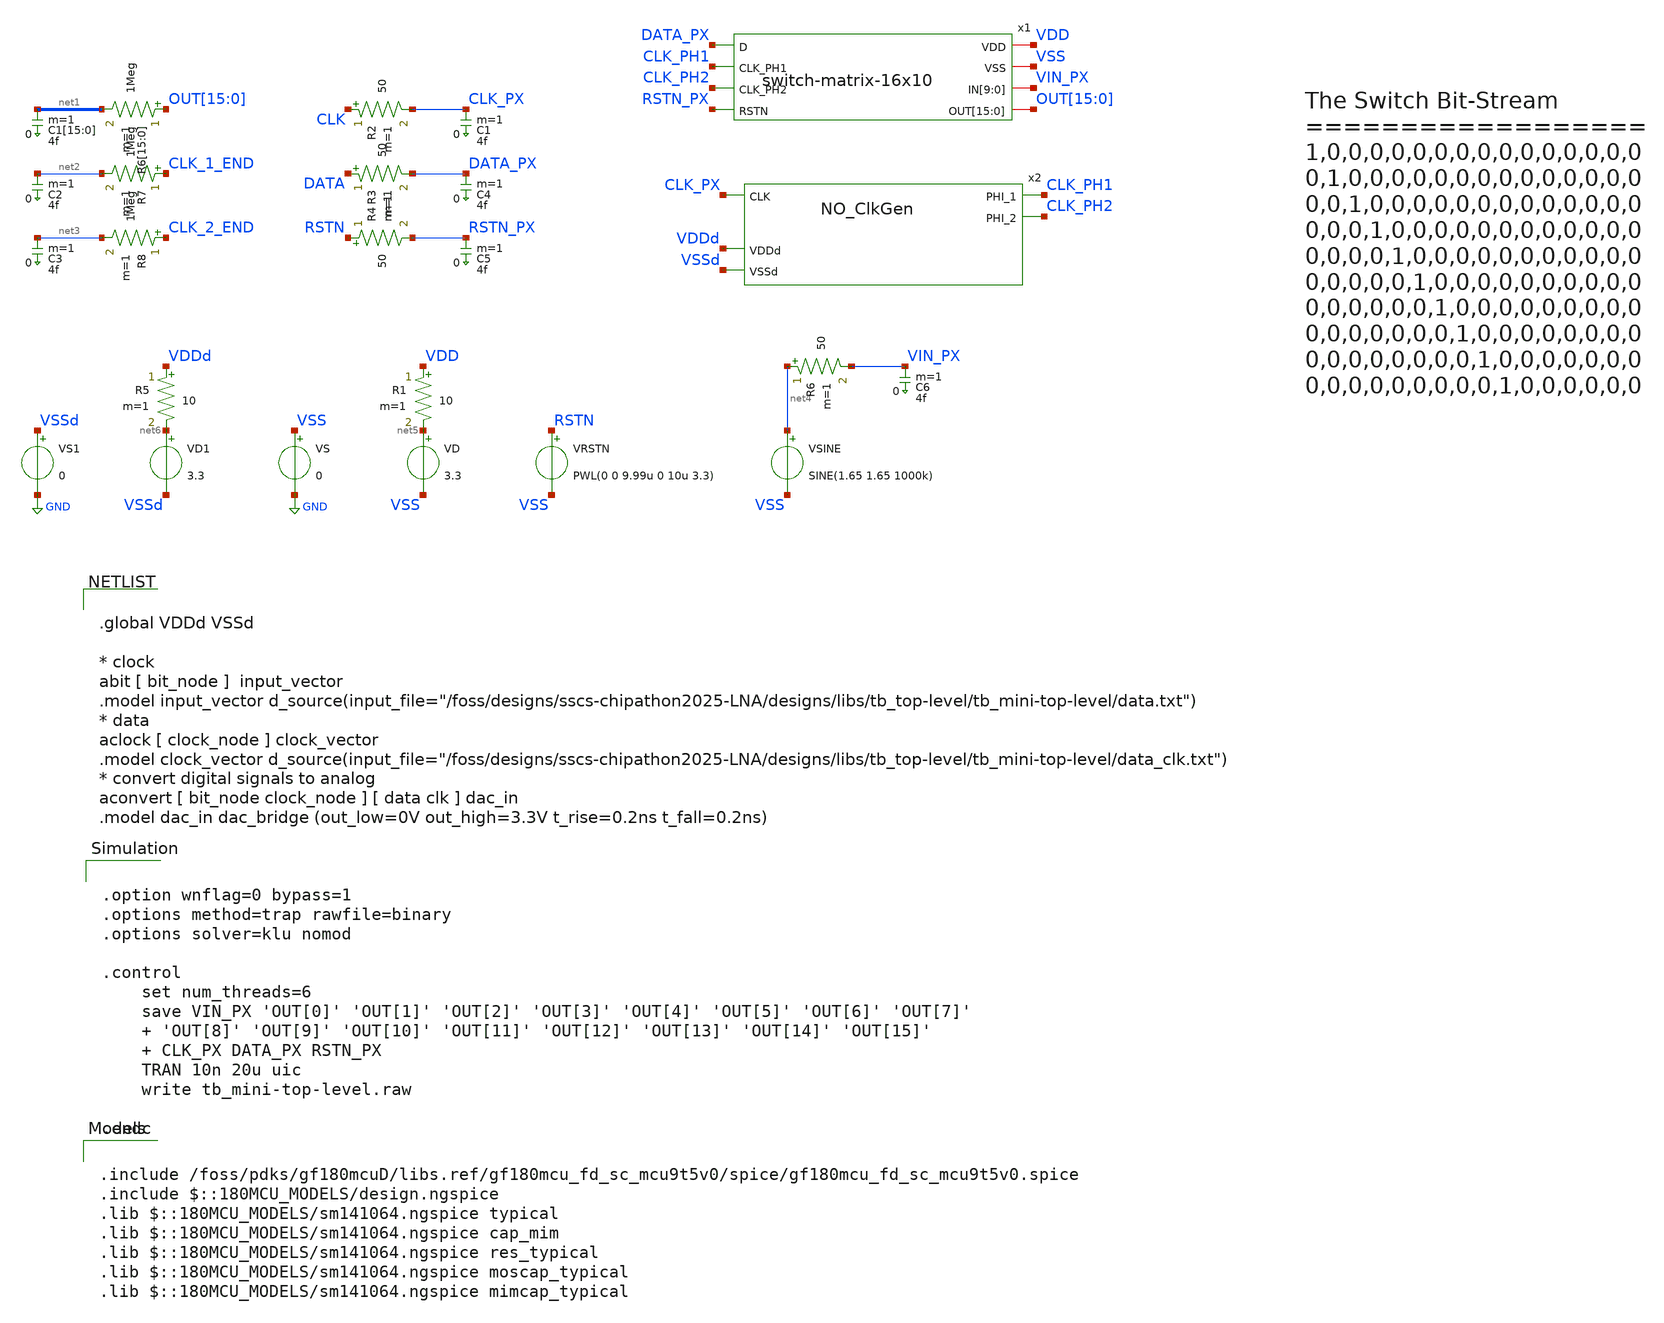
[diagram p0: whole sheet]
** sch_path: designs/libs/tb_top-level/tb_mini-top-level/tb_mini-top-level.sch
**.subckt tb_mini-top-level
x2 CLK_PH2 CLK_PX CLK_PH1 VDDd VSSd NO_ClkGen
VD net5 VSS 3.3
R1 VDD net5 10 m=1
R2 CLK CLK_PX 50 m=1
R3 DATA DATA_PX 50 m=1
VS VSS GND 0
VRSTN RSTN VSS PWL(0 0 9.99u 0 10u 3.3)
R4 RSTN RSTN_PX 50 m=1
VD1 net6 VSSd 3.3
R5 VDDd net6 10 m=1
VS1 VSSd GND 0
C1[15] net1[15] 0 4f m=1
C1[14] net1[14] 0 4f m=1
C1[13] net1[13] 0 4f m=1
C1[12] net1[12] 0 4f m=1
C1[11] net1[11] 0 4f m=1
C1[10] net1[10] 0 4f m=1
C1[9] net1[9] 0 4f m=1
C1[8] net1[8] 0 4f m=1
C1[7] net1[7] 0 4f m=1
C1[6] net1[6] 0 4f m=1
C1[5] net1[5] 0 4f m=1
C1[4] net1[4] 0 4f m=1
C1[3] net1[3] 0 4f m=1
C1[2] net1[2] 0 4f m=1
C1[1] net1[1] 0 4f m=1
C1[0] net1[0] 0 4f m=1
C2 net2 0 4f m=1
C3 net3 0 4f m=1
C1 CLK_PX 0 4f m=1
C4 DATA_PX 0 4f m=1
R6[15] OUT[15] net1[15] 1Meg m=1
R6[14] OUT[14] net1[14] 1Meg m=1
R6[13] OUT[13] net1[13] 1Meg m=1
R6[12] OUT[12] net1[12] 1Meg m=1
R6[11] OUT[11] net1[11] 1Meg m=1
R6[10] OUT[10] net1[10] 1Meg m=1
R6[9] OUT[9] net1[9] 1Meg m=1
R6[8] OUT[8] net1[8] 1Meg m=1
R6[7] OUT[7] net1[7] 1Meg m=1
R6[6] OUT[6] net1[6] 1Meg m=1
R6[5] OUT[5] net1[5] 1Meg m=1
R6[4] OUT[4] net1[4] 1Meg m=1
R6[3] OUT[3] net1[3] 1Meg m=1
R6[2] OUT[2] net1[2] 1Meg m=1
R6[1] OUT[1] net1[1] 1Meg m=1
R6[0] OUT[0] net1[0] 1Meg m=1
R7 CLK_1_END net2 1Meg m=1
R8 CLK_2_END net3 1Meg m=1
C5 RSTN_PX 0 4f m=1
VSINE net4 VSS SINE(1.65 1.65 1000k)
R6 net4 VIN_PX 50 m=1
C6 VIN_PX 0 4f m=1
x1 DATA_PX CLK_PH1 CLK_PH2 RSTN_PX VDD VSS VIN_PX VIN_PX VIN_PX VIN_PX VIN_PX VIN_PX VIN_PX VIN_PX
+ VIN_PX VIN_PX OUT[15] OUT[14] OUT[13] OUT[12] OUT[11] OUT[10] OUT[9] OUT[8] OUT[7] OUT[6] OUT[5] OUT[4]
+ OUT[3] OUT[2] OUT[1] OUT[0] switch-matrix-16x10
**** begin user architecture code


.option wnflag=0 bypass=1
.options method=trap rawfile=binary
.options solver=klu nomod

.control
    set num_threads=6
    save VIN_PX 'OUT[0]' 'OUT[1]' 'OUT[2]' 'OUT[3]' 'OUT[4]' 'OUT[5]' 'OUT[6]' 'OUT[7]'
    + 'OUT[8]' 'OUT[9]' 'OUT[10]' 'OUT[11]' 'OUT[12]' 'OUT[13]' 'OUT[14]' 'OUT[15]'
    + CLK_PX DATA_PX RSTN_PX
    TRAN 10n 20u uic
    write tb_mini-top-level.raw

.endc



.include /foss/pdks/gf180mcuD/libs.ref/gf180mcu_fd_sc_mcu9t5v0/spice/gf180mcu_fd_sc_mcu9t5v0.spice
.include $::180MCU_MODELS/design.ngspice
.lib $::180MCU_MODELS/sm141064.ngspice typical
.lib $::180MCU_MODELS/sm141064.ngspice cap_mim
.lib $::180MCU_MODELS/sm141064.ngspice res_typical
.lib $::180MCU_MODELS/sm141064.ngspice moscap_typical
.lib $::180MCU_MODELS/sm141064.ngspice mimcap_typical



.global VDDd VSSd

* clock
abit [ bit_node ]  input_vector
.model input_vector
+ d_source(input_file="/foss/designs/sscs-chipathon2025-LNA/designs/libs/tb_top-level/tb_mini-top-level/data.txt")
* data
aclock [ clock_node ] clock_vector
.model clock_vector
+ d_source(input_file="/foss/designs/sscs-chipathon2025-LNA/designs/libs/tb_top-level/tb_mini-top-level/data_clk.txt")
* convert digital signals to analog
aconvert [ bit_node clock_node ] [ data clk ] dac_in
.model dac_in dac_bridge (out_low=0V out_high=3.3V t_rise=0.2ns t_fall=0.2ns)


**** end user architecture code
**.ends
.GLOBAL GND
.end
